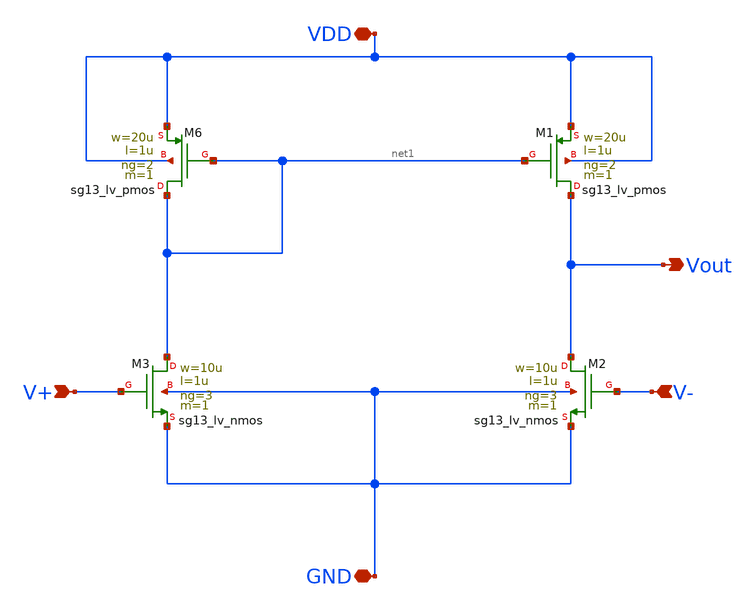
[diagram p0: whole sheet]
** sch_path: SSDOR_1.2V_v2/components/Ib_4u/Ib_4u_opamp/Ib_4u_opamp.sch
**.subckt Ib_4u_opamp VDD V+ V- GND Vout
*.iopin VDD
*.ipin V+
*.ipin V-
*.iopin GND
*.opin Vout
XM6 net1 net1 VDD VDD sg13_lv_pmos w=20u l=1u ng=2 m=1 mm_ok=1
XM3 net1 V+ GND GND sg13_lv_nmos w=10u l=1u ng=3 m=1 mm_ok=1
XM2 Vout V- GND GND sg13_lv_nmos w=10u l=1u ng=3 m=1 mm_ok=1
XM1 Vout net1 VDD VDD sg13_lv_pmos w=20u l=1u ng=2 m=1 mm_ok=1
**.ends
.end
